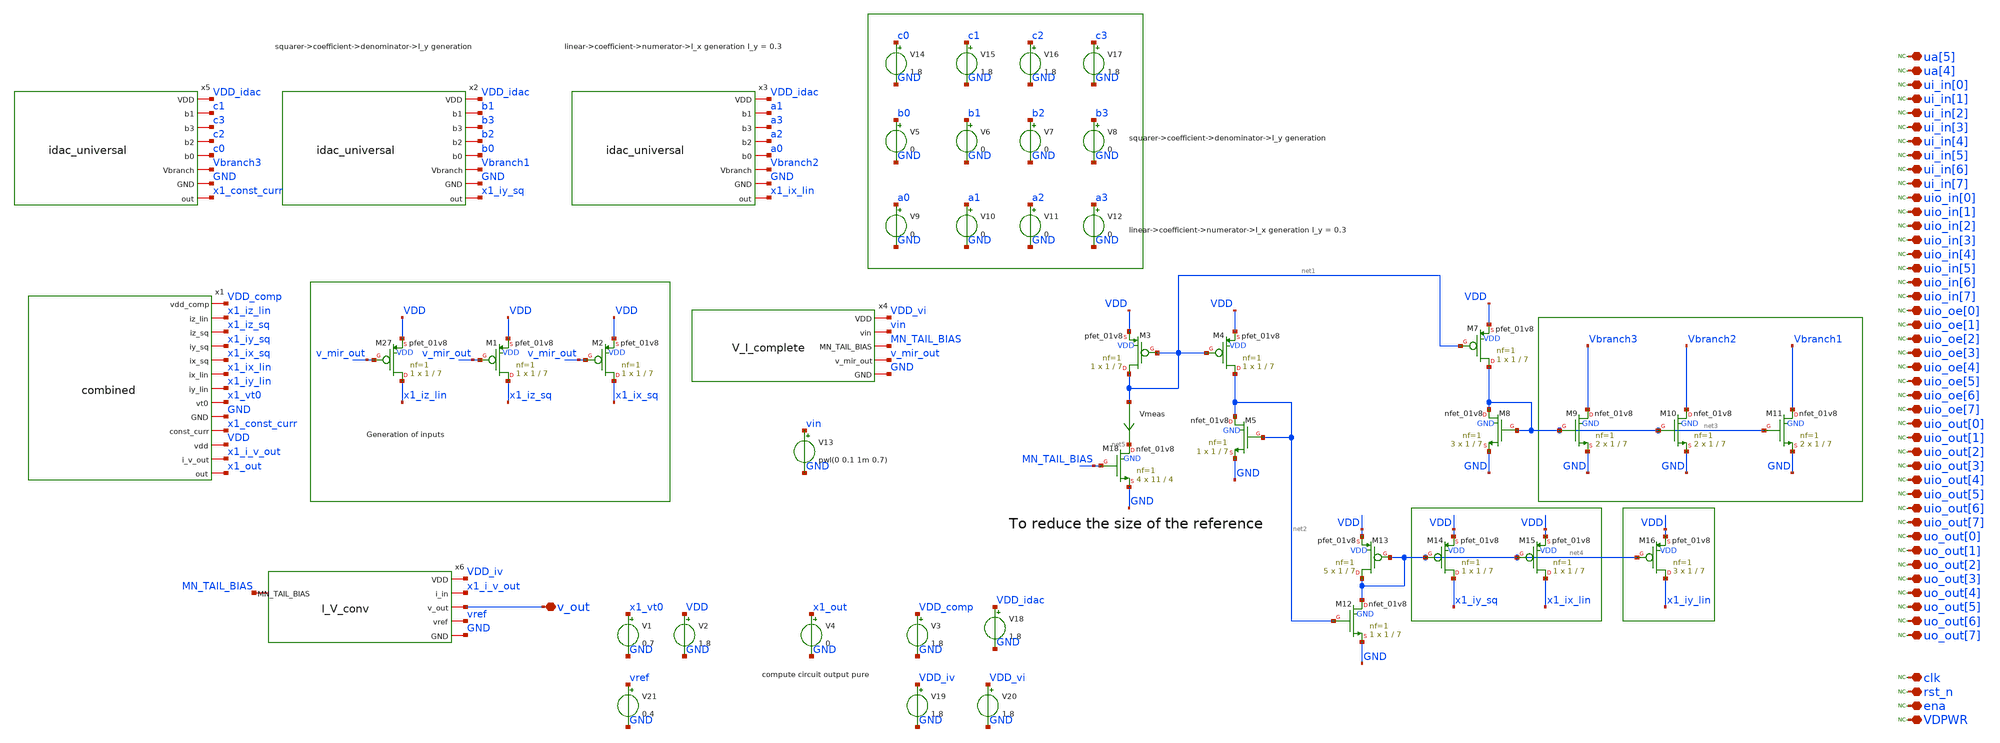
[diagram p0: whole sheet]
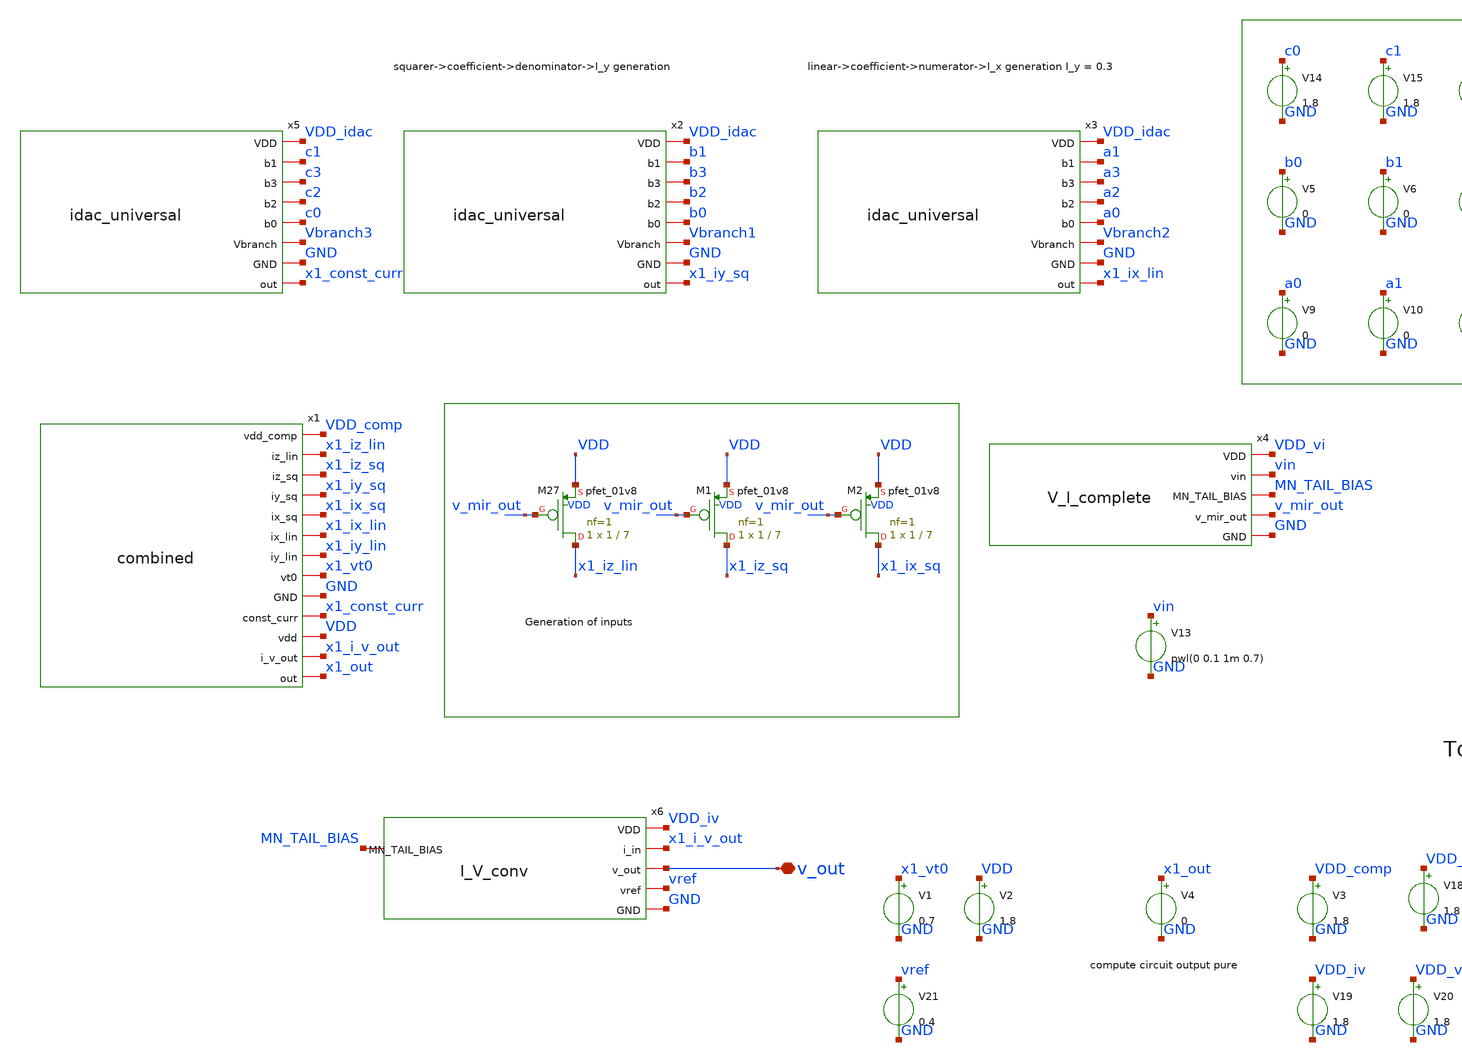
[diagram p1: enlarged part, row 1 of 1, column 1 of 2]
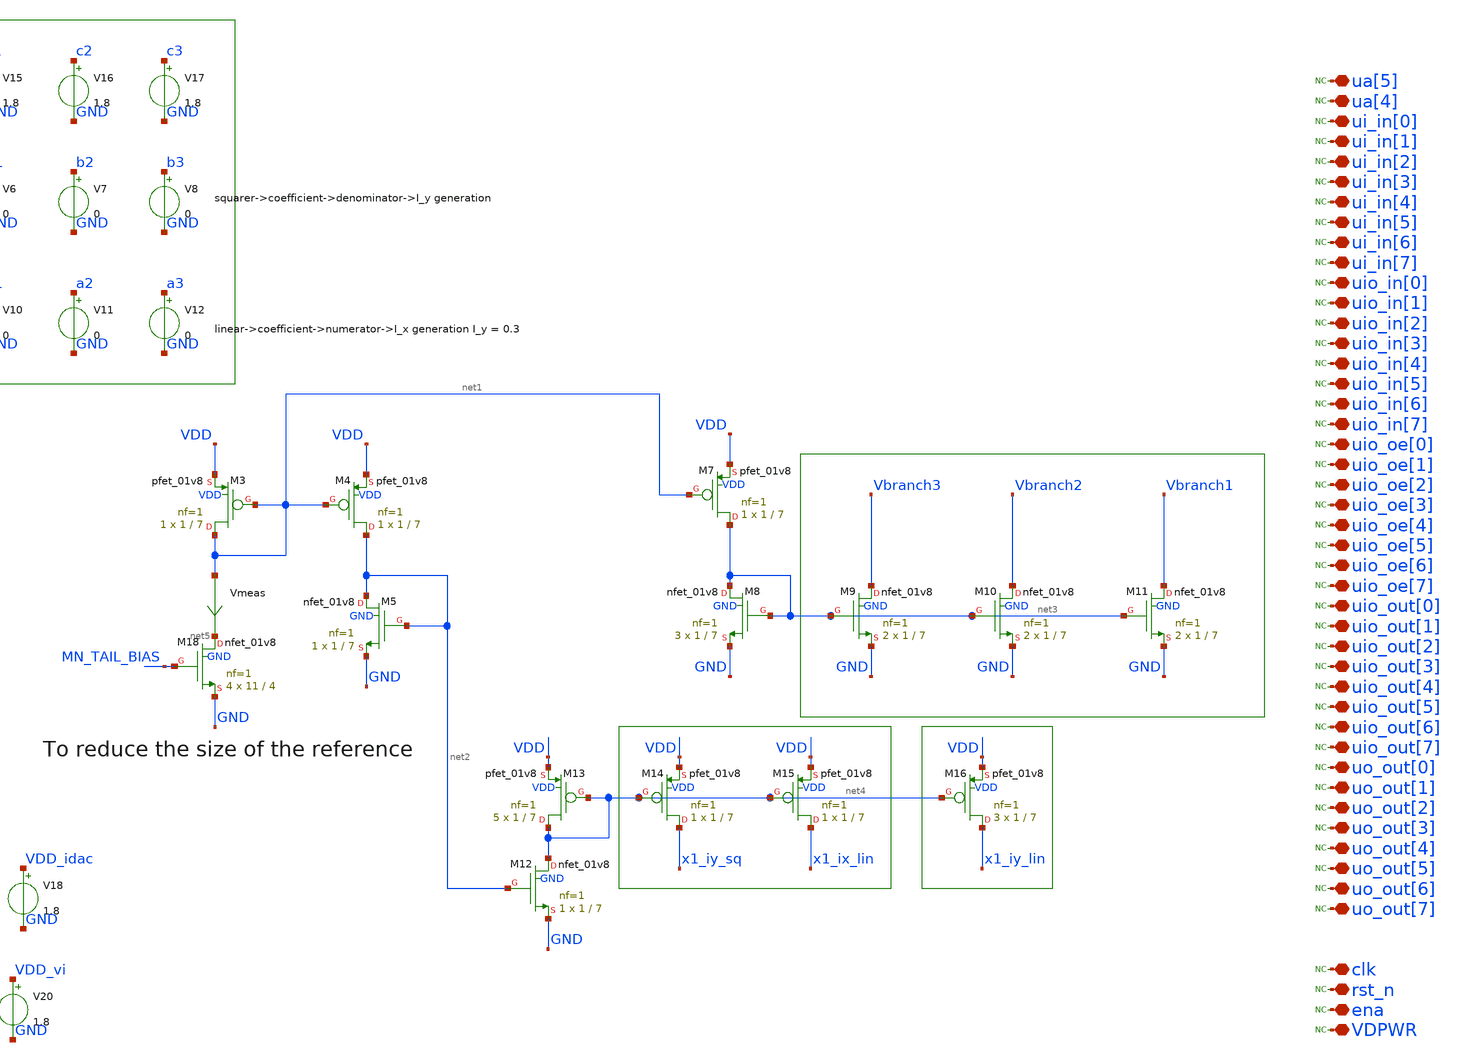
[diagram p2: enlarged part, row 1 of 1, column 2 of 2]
** sch_path: xschem/tb/IDAC_poly_V_I.sch
**.subckt IDAC_poly_V_I v_out ui_in[4] ui_in[5] ui_in[6] ui_in[7] uio_in[0] uio_in[1] uio_in[2]
*+ uio_in[3] uio_in[4] uio_in[5] uio_in[6] uio_in[7] uio_oe[0] uio_oe[1] uio_oe[2] uio_oe[3] uio_oe[4] uio_oe[5]
*+ uio_oe[6] uio_oe[7] uio_out[0] uio_out[1] uio_out[2] uio_out[3] uio_out[4] uio_out[5] uio_out[6] uio_out[7]
*+ uo_out[0] uo_out[1] uo_out[2] uo_out[3] uo_out[4] uo_out[5] uo_out[6] uo_out[7] clk rst_n ena ua[4] ua[5]
*+ ui_in[0] ui_in[3] ui_in[1] ui_in[2] VDPWR
*.iopin v_out
*.iopin ui_in[4]
*.iopin ui_in[5]
*.iopin ui_in[6]
*.iopin ui_in[7]
*.iopin uio_in[0]
*.iopin uio_in[1]
*.iopin uio_in[2]
*.iopin uio_in[3]
*.iopin uio_in[4]
*.iopin uio_in[5]
*.iopin uio_in[6]
*.iopin uio_in[7]
*.iopin uio_oe[0]
*.iopin uio_oe[1]
*.iopin uio_oe[2]
*.iopin uio_oe[3]
*.iopin uio_oe[4]
*.iopin uio_oe[5]
*.iopin uio_oe[6]
*.iopin uio_oe[7]
*.iopin uio_out[0]
*.iopin uio_out[1]
*.iopin uio_out[2]
*.iopin uio_out[3]
*.iopin uio_out[4]
*.iopin uio_out[5]
*.iopin uio_out[6]
*.iopin uio_out[7]
*.iopin uo_out[0]
*.iopin uo_out[1]
*.iopin uo_out[2]
*.iopin uo_out[3]
*.iopin uo_out[4]
*.iopin uo_out[5]
*.iopin uo_out[6]
*.iopin uo_out[7]
*.iopin clk
*.iopin rst_n
*.iopin ena
*.iopin ua[4]
*.iopin ua[5]
*.iopin ui_in[0]
*.iopin ui_in[3]
*.iopin ui_in[1]
*.iopin ui_in[2]
*.iopin VDPWR
V5 b0 GND 0
V6 b1 GND 0
V7 b2 GND 0
V8 b3 GND 0
V9 a0 GND 0
V10 a1 GND 0
V11 a2 GND 0
V12 a3 GND 0
V1 x1_vt0 GND 0.7
V2 VDD GND 1.8
V4 x1_out GND 0
XM27 x1_iz_lin v_mir_out VDD VDD sky130_fd_pr__pfet_01v8 L=7 W=1 nf=1 ad='int((1 + 1)/2) * 1 / 1 * 0.29'
+ as='int((1 + 2)/2) * 1 / 1 * 0.29' pd='2*int((1 + 1)/2) * (1 / 1 + 0.29)' ps='2*int((1 + 2)/2) * (1 / 1 + 0.29)'
+ nrd='0.29 / 1 ' nrs='0.29 / 1 ' sa=0 sb=0 sd=0 mult=1 m=1
XM1 x1_iz_sq v_mir_out VDD VDD sky130_fd_pr__pfet_01v8 L=7 W=1 nf=1 ad='int((1 + 1)/2) * 1 / 1 * 0.29'
+ as='int((1 + 2)/2) * 1 / 1 * 0.29' pd='2*int((1 + 1)/2) * (1 / 1 + 0.29)' ps='2*int((1 + 2)/2) * (1 / 1 + 0.29)'
+ nrd='0.29 / 1 ' nrs='0.29 / 1 ' sa=0 sb=0 sd=0 mult=1 m=1
XM2 x1_ix_sq v_mir_out VDD VDD sky130_fd_pr__pfet_01v8 L=7 W=1 nf=1 ad='int((1 + 1)/2) * 1 / 1 * 0.29'
+ as='int((1 + 2)/2) * 1 / 1 * 0.29' pd='2*int((1 + 1)/2) * (1 / 1 + 0.29)' ps='2*int((1 + 2)/2) * (1 / 1 + 0.29)'
+ nrd='0.29 / 1 ' nrs='0.29 / 1 ' sa=0 sb=0 sd=0 mult=1 m=1
V14 c0 GND 1.8
V15 c1 GND 1.8
V16 c2 GND 1.8
V17 c3 GND 1.8
XM18 net5 MN_TAIL_BIAS GND GND sky130_fd_pr__nfet_01v8 L=4 W=11 nf=1 ad='int((nf+1)/2) * W/nf * 0.29'
+ as='int((nf+2)/2) * W/nf * 0.29' pd='2*int((nf+1)/2) * (W/nf + 0.29)' ps='2*int((nf+2)/2) * (W/nf + 0.29)'
+ nrd='0.29 / W' nrs='0.29 / W' sa=0 sb=0 sd=0 mult=4 m=4
XM3 net1 net1 VDD VDD sky130_fd_pr__pfet_01v8 L=7 W=1 nf=1 ad='int((1 + 1)/2) * 1 / 1 * 0.29' as='int((1 + 2)/2) * 1 / 1 * 0.29'
+ pd='2*int((1 + 1)/2) * (1 / 1 + 0.29)' ps='2*int((1 + 2)/2) * (1 / 1 + 0.29)' nrd='0.29 / 1 ' nrs='0.29 / 1 '
+ sa=0 sb=0 sd=0 mult=1 m=1
XM4 net2 net1 VDD VDD sky130_fd_pr__pfet_01v8 L=7 W=1 nf=1 ad='int((1 + 1)/2) * 1 / 1 * 0.29' as='int((1 + 2)/2) * 1 / 1 * 0.29'
+ pd='2*int((1 + 1)/2) * (1 / 1 + 0.29)' ps='2*int((1 + 2)/2) * (1 / 1 + 0.29)' nrd='0.29 / 1 ' nrs='0.29 / 1 '
+ sa=0 sb=0 sd=0 mult=1 m=1
XM5 net2 net2 GND GND sky130_fd_pr__nfet_01v8 L=7 W=1 nf=1 ad='int((nf+1)/2) * W/nf * 0.29' as='int((nf+2)/2) * W/nf * 0.29'
+ pd='2*int((nf+1)/2) * (W/nf + 0.29)' ps='2*int((nf+2)/2) * (W/nf + 0.29)' nrd='0.29 / W' nrs='0.29 / W'
+ sa=0 sb=0 sd=0 mult=1 m=1
Vmeas net1 net5 0
.save i(vmeas)
XM7 net3 net1 VDD VDD sky130_fd_pr__pfet_01v8 L=7 W=1 nf=1 ad='int((1 + 1)/2) * 1 / 1 * 0.29' as='int((1 + 2)/2) * 1 / 1 * 0.29'
+ pd='2*int((1 + 1)/2) * (1 / 1 + 0.29)' ps='2*int((1 + 2)/2) * (1 / 1 + 0.29)' nrd='0.29 / 1 ' nrs='0.29 / 1 '
+ sa=0 sb=0 sd=0 mult=1 m=1
XM8 net3 net3 GND GND sky130_fd_pr__nfet_01v8 L=7 W=1 nf=1 ad='int((nf+1)/2) * W/nf * 0.29' as='int((nf+2)/2) * W/nf * 0.29'
+ pd='2*int((nf+1)/2) * (W/nf + 0.29)' ps='2*int((nf+2)/2) * (W/nf + 0.29)' nrd='0.29 / W' nrs='0.29 / W'
+ sa=0 sb=0 sd=0 mult=3 m=3
XM9 Vbranch3 net3 GND GND sky130_fd_pr__nfet_01v8 L=7 W=1 nf=1 ad='int((nf+1)/2) * W/nf * 0.29' as='int((nf+2)/2) * W/nf * 0.29'
+ pd='2*int((nf+1)/2) * (W/nf + 0.29)' ps='2*int((nf+2)/2) * (W/nf + 0.29)' nrd='0.29 / W' nrs='0.29 / W'
+ sa=0 sb=0 sd=0 mult=2 m=2
XM10 Vbranch2 net3 GND GND sky130_fd_pr__nfet_01v8 L=7 W=1 nf=1 ad='int((nf+1)/2) * W/nf * 0.29' as='int((nf+2)/2) * W/nf * 0.29'
+ pd='2*int((nf+1)/2) * (W/nf + 0.29)' ps='2*int((nf+2)/2) * (W/nf + 0.29)' nrd='0.29 / W' nrs='0.29 / W'
+ sa=0 sb=0 sd=0 mult=2 m=2
XM11 Vbranch1 net3 GND GND sky130_fd_pr__nfet_01v8 L=7 W=1 nf=1 ad='int((nf+1)/2) * W/nf * 0.29' as='int((nf+2)/2) * W/nf * 0.29'
+ pd='2*int((nf+1)/2) * (W/nf + 0.29)' ps='2*int((nf+2)/2) * (W/nf + 0.29)' nrd='0.29 / W' nrs='0.29 / W'
+ sa=0 sb=0 sd=0 mult=2 m=2
XM12 net4 net2 GND GND sky130_fd_pr__nfet_01v8 L=7 W=1 nf=1 ad='int((nf+1)/2) * W/nf * 0.29' as='int((nf+2)/2) * W/nf * 0.29'
+ pd='2*int((nf+1)/2) * (W/nf + 0.29)' ps='2*int((nf+2)/2) * (W/nf + 0.29)' nrd='0.29 / W' nrs='0.29 / W'
+ sa=0 sb=0 sd=0 mult=1 m=1
XM13 net4 net4 VDD VDD sky130_fd_pr__pfet_01v8 L=7 W=1 nf=1 ad='int((1 + 1)/2) * 1 / 1 * 0.29' as='int((1 + 2)/2) * 1 / 1 * 0.29'
+ pd='2*int((1 + 1)/2) * (1 / 1 + 0.29)' ps='2*int((1 + 2)/2) * (1 / 1 + 0.29)' nrd='0.29 / 1 ' nrs='0.29 / 1 '
+ sa=0 sb=0 sd=0 mult=5 m=5
XM14 x1_iy_sq net4 VDD VDD sky130_fd_pr__pfet_01v8 L=7 W=1 nf=1 ad='int((1 + 1)/2) * 1 / 1 * 0.29' as='int((1 + 2)/2) * 1 / 1 * 0.29'
+ pd='2*int((1 + 1)/2) * (1 / 1 + 0.29)' ps='2*int((1 + 2)/2) * (1 / 1 + 0.29)' nrd='0.29 / 1 ' nrs='0.29 / 1 '
+ sa=0 sb=0 sd=0 mult=1 m=1
XM15 x1_ix_lin net4 VDD VDD sky130_fd_pr__pfet_01v8 L=7 W=1 nf=1 ad='int((1 + 1)/2) * 1 / 1 * 0.29' as='int((1 + 2)/2) * 1 / 1 * 0.29'
+ pd='2*int((1 + 1)/2) * (1 / 1 + 0.29)' ps='2*int((1 + 2)/2) * (1 / 1 + 0.29)' nrd='0.29 / 1 ' nrs='0.29 / 1 '
+ sa=0 sb=0 sd=0 mult=1 m=1
XM16 x1_iy_lin net4 VDD VDD sky130_fd_pr__pfet_01v8 L=7 W=1 nf=1 ad='int((1 + 1)/2) * 1 / 1 * 0.29' as='int((1 + 2)/2) * 1 / 1 * 0.29'
+ pd='2*int((1 + 1)/2) * (1 / 1 + 0.29)' ps='2*int((1 + 2)/2) * (1 / 1 + 0.29)' nrd='0.29 / 1 ' nrs='0.29 / 1 '
+ sa=0 sb=0 sd=0 mult=3 m=3
x5 VDD_idac c1 c3 c2 c0 Vbranch3 GND x1_const_curr idac_universal
x2 VDD_idac b1 b3 b2 b0 Vbranch1 GND x1_iy_sq idac_universal
x3 VDD_idac a1 a3 a2 a0 Vbranch2 GND x1_ix_lin idac_universal
x1 VDD_comp x1_iz_lin x1_iz_sq x1_iy_sq x1_ix_sq x1_ix_lin x1_iy_lin x1_vt0 GND x1_const_curr VDD
+ x1_i_v_out x1_out combined
x6 VDD_iv x1_i_v_out v_out vref GND MN_TAIL_BIAS I_V_conv
x4 VDD_vi vin MN_TAIL_BIAS v_mir_out GND V_I_complete
V3 VDD_comp GND 1.8
V18 VDD_idac GND 1.8
V19 VDD_iv GND 1.8
V20 VDD_vi GND 1.8
V21 vref GND 0.4
V13 vin GND pwl(0 0.1 1m 0.7)
* noconn ua[5]
* noconn ua[4]
* noconn ui_in[0]
* noconn ui_in[1]
* noconn ui_in[2]
* noconn ui_in[3]
* noconn ui_in[4]
* noconn ui_in[5]
* noconn ui_in[6]
* noconn ui_in[7]
* noconn uio_in[0]
* noconn uio_in[1]
* noconn uio_in[2]
* noconn uio_in[3]
* noconn uio_in[4]
* noconn uio_in[5]
* noconn uio_in[6]
* noconn uio_in[7]
* noconn uio_oe[0]
* noconn uio_oe[1]
* noconn uio_oe[2]
* noconn uio_oe[3]
* noconn uio_oe[4]
* noconn uio_oe[5]
* noconn uio_oe[6]
* noconn uio_oe[7]
* noconn uio_out[0]
* noconn uio_out[1]
* noconn uio_out[2]
* noconn uio_out[3]
* noconn uio_out[4]
* noconn uio_out[5]
* noconn uio_out[6]
* noconn uio_out[7]
* noconn uo_out[0]
* noconn uo_out[1]
* noconn uo_out[2]
* noconn uo_out[3]
* noconn uo_out[4]
* noconn uo_out[5]
* noconn uo_out[6]
* noconn uo_out[7]
* noconn clk
* noconn rst_n
* noconn ena
* noconn VDPWR
**** begin user architecture code


.options savecurrents
.options rshunt=1e12 method=gear
*.options reltol=1e-3 abstol=1e-12
.control

save all
* dc V13 0 0.7 0.005
tran 1u 1m
set filetype=ascii
write IDAC_poly_V_I.raw
plot v(v_out)
plot @m.xm1.msky130_fd_pr__pfet_01v8[id]
plot i(v4)
.endc



** opencircuitdesign pdks install
.lib $::SKYWATER_MODELS/sky130.lib.spice tt

**** end user architecture code
**.ends
.end
